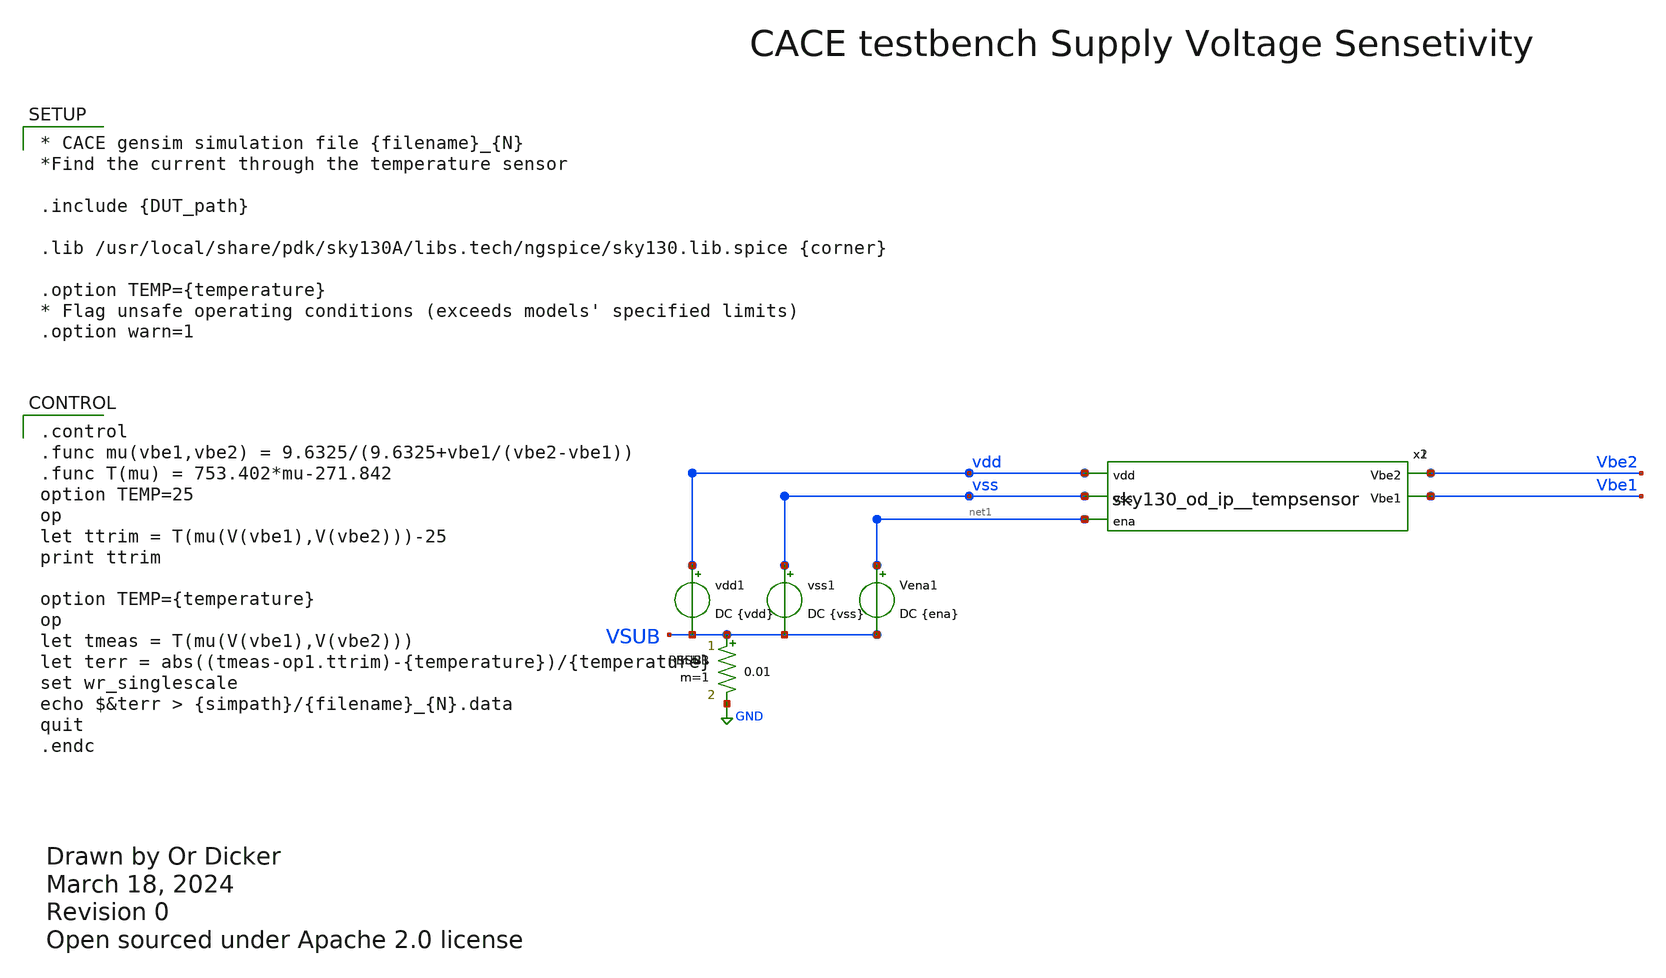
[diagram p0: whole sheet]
** sch_path: cace/supply_sens.sch
* Open sourced under Apache 2.0 license
**.subckt supply_sens
vss vss VSUB DC {vss}
vdd vdd VSUB DC {vdd}
RSUB VSUB GND 0.01 m=1
x1 vdd vss Vbe2 Vbe1 net1 sky130_od_ip__tempsensor
Vena net1 VSUB DC {ena}
vss1 vss VSUB DC {vss}
vdd1 vdd VSUB DC {vdd}
RSUB1 VSUB GND 0.01 m=1
x2 vdd vss Vbe2 Vbe1 net1 sky130_od_ip__tempsensor
Vena1 net1 VSUB DC {ena}
**** begin user architecture code

.control
.func mu(vbe1,vbe2) = 9.6325/(9.6325+vbe1/(vbe2-vbe1))
.func T(mu) = 753.402*mu-271.842
option TEMP=25
op
let ttrim = T(mu(V(vbe1),V(vbe2)))-25
print ttrim

option TEMP={temperature}
op
let tmeas = T(mu(V(vbe1),V(vbe2)))
let terr = abs((tmeas-op1.ttrim)-{temperature})/{temperature}
set wr_singlescale
echo $&terr > {simpath}/{filename}_{N}.data
quit
.endc



* CACE gensim simulation file {filename}_{N}
*Find the current through the temperature sensor

.include {DUT_path}

.lib /usr/local/share/pdk/sky130A/libs.tech/ngspice/sky130.lib.spice {corner}

.option TEMP={temperature}
* Flag unsafe operating conditions (exceeds models' specified limits)
.option warn=1


**** end user architecture code
**.ends

* expanding   symbol:  xschem/sky130_od_ip__tempsensor.sym # of pins=5
** sym_path: xschem/sky130_od_ip__tempsensor.sym
** sch_path: xschem/sky130_od_ip__tempsensor.sch
.subckt sky130_od_ip__tempsensor vdd vss Vbe2 Vbe1 ena
*.ipin vdd
*.ipin vss
*.opin Vbe2
*.opin Vbe1
*.ipin ena
XM12 net1 Vp vdd vdd sky130_fd_pr__pfet_01v8 L=1.2 W=1 nf=1 ad='int((nf+1)/2) * W/nf * 0.29' as='int((nf+2)/2)
+ * W/nf * 0.29' pd='2*int((nf+1)/2) * (W/nf + 0.29)' ps='2*int((nf+2)/2) * (W/nf + 0.29)' nrd='0.29 /
+ W' nrs='0.29 / W' sa=0 sb=0 sd=0 mult=5 m=5
XM13 net2 Vp vdd vdd sky130_fd_pr__pfet_01v8 L=1.2 W=1 nf=1 ad='int((nf+1)/2) * W/nf * 0.29' as='int((nf+2)/2)
+ * W/nf * 0.29' pd='2*int((nf+1)/2) * (W/nf + 0.29)' ps='2*int((nf+2)/2) * (W/nf + 0.29)' nrd='0.29 /
+ W' nrs='0.29 / W' sa=0 sb=0 sd=0 mult=1 m=1
XQ_BR vss net3 net1 sky130_fd_pr__pnp_05v5_W3p40L3p40 m=1
XQ_BL vss vss net4 sky130_fd_pr__pnp_05v5_W3p40L3p40 m=1
Rb net2 net4 5k m=1
Rb_5 net3 vss 1k m=1
XM11 net5 Vp vdd vdd sky130_fd_pr__pfet_01v8 L=1.2 W=1 nf=1 ad='int((nf+1)/2) * W/nf * 0.29' as='int((nf+2)/2)
+ * W/nf * 0.29' pd='2*int((nf+1)/2) * (W/nf + 0.29)' ps='2*int((nf+2)/2) * (W/nf + 0.29)' nrd='0.29 /
+ W' nrs='0.29 / W' sa=0 sb=0 sd=0 mult=2 m=2
XM6 net6 net2 net5 net5 sky130_fd_pr__pfet_01v8 L=1.2 W=10 nf=1 ad='int((nf+1)/2) * W/nf * 0.29' as='int((nf+2)/2)
+ * W/nf * 0.29' pd='2*int((nf+1)/2) * (W/nf + 0.29)' ps='2*int((nf+2)/2) * (W/nf + 0.29)' nrd='0.29 /
+ W' nrs='0.29 / W' sa=0 sb=0 sd=0 mult=1 m=1
XM5 net7 net1 net5 net5 sky130_fd_pr__pfet_01v8 L=1.2 W=10 nf=1 ad='int((nf+1)/2) * W/nf * 0.29' as='int((nf+2)/2)
+ * W/nf * 0.29' pd='2*int((nf+1)/2) * (W/nf + 0.29)' ps='2*int((nf+2)/2) * (W/nf + 0.29)' nrd='0.29 /
+ W' nrs='0.29 / W' sa=0 sb=0 sd=0 mult=1 m=1
XM2 net6 net7 vss vss sky130_fd_pr__nfet_01v8 L=1.2 W=10 nf=1 ad='int((nf+1)/2) * W/nf * 0.29' as='int((nf+2)/2)
+ * W/nf * 0.29' pd='2*int((nf+1)/2) * (W/nf + 0.29)' ps='2*int((nf+2)/2) * (W/nf + 0.29)' nrd='0.29 /
+ W' nrs='0.29 / W' sa=0 sb=0 sd=0 mult=1 m=1
XM1 net7 net7 vss vss sky130_fd_pr__nfet_01v8 L=1.2 W=10 nf=1 ad='int((nf+1)/2) * W/nf * 0.29' as='int((nf+2)/2)
+ * W/nf * 0.29' pd='2*int((nf+1)/2) * (W/nf + 0.29)' ps='2*int((nf+2)/2) * (W/nf + 0.29)' nrd='0.29 /
+ W' nrs='0.29 / W' sa=0 sb=0 sd=0 mult=1 m=1
XM9 net8 Vp vdd vdd sky130_fd_pr__pfet_01v8 L=1.2 W=1 nf=1 ad='int((nf+1)/2) * W/nf * 0.29' as='int((nf+2)/2)
+ * W/nf * 0.29' pd='2*int((nf+1)/2) * (W/nf + 0.29)' ps='2*int((nf+2)/2) * (W/nf + 0.29)' nrd='0.29 /
+ W' nrs='0.29 / W' sa=0 sb=0 sd=0 mult=1 m=1
XM10 Vp Vp vdd vdd sky130_fd_pr__pfet_01v8 L=1.2 W=1 nf=1 ad='int((nf+1)/2) * W/nf * 0.29' as='int((nf+2)/2)
+ * W/nf * 0.29' pd='2*int((nf+1)/2) * (W/nf + 0.29)' ps='2*int((nf+2)/2) * (W/nf + 0.29)' nrd='0.29 /
+ W' nrs='0.29 / W' sa=0 sb=0 sd=0 mult=4 m=4
XM7 Vp net8 net10 net10 sky130_fd_pr__nfet_01v8 L=1.2 W=10 nf=1 ad='int((nf+1)/2) * W/nf * 0.29' as='int((nf+2)/2)
+ * W/nf * 0.29' pd='2*int((nf+1)/2) * (W/nf + 0.29)' ps='2*int((nf+2)/2) * (W/nf + 0.29)' nrd='0.29 /
+ W' nrs='0.29 / W' sa=0 sb=0 sd=0 mult=1 m=1
XM8 net8 net8 net9 net9 sky130_fd_pr__nfet_01v8 L=1.2 W=10 nf=1 ad='int((nf+1)/2) * W/nf * 0.29' as='int((nf+2)/2)
+ * W/nf * 0.29' pd='2*int((nf+1)/2) * (W/nf + 0.29)' ps='2*int((nf+2)/2) * (W/nf + 0.29)' nrd='0.29 /
+ W' nrs='0.29 / W' sa=0 sb=0 sd=0 mult=1 m=1
XM3 net10 net6 vss vss sky130_fd_pr__nfet_01v8 L=1.2 W=10 nf=1 ad='int((nf+1)/2) * W/nf * 0.29' as='int((nf+2)/2)
+ * W/nf * 0.29' pd='2*int((nf+1)/2) * (W/nf + 0.29)' ps='2*int((nf+2)/2) * (W/nf + 0.29)' nrd='0.29 /
+ W' nrs='0.29 / W' sa=0 sb=0 sd=0 mult=4 m=4
XM4 net9 net9 vss vss sky130_fd_pr__nfet_01v8 L=1.2 W=1 nf=1 ad='int((nf+1)/2) * W/nf * 0.29' as='int((nf+2)/2)
+ * W/nf * 0.29' pd='2*int((nf+1)/2) * (W/nf + 0.29)' ps='2*int((nf+2)/2) * (W/nf + 0.29)' nrd='0.29 /
+ W' nrs='0.29 / W' sa=0 sb=0 sd=0 mult=20 m=20
XQ_BL1 vss vss Vbe1 sky130_fd_pr__pnp_05v5_W3p40L3p40 m=1
XQ_BR1 vss vss Vbe2 sky130_fd_pr__pnp_05v5_W3p40L3p40 m=1
XM14 Vbe1 Vp vdd vdd sky130_fd_pr__pfet_01v8 L=1.2 W=1 nf=1 ad='int((nf+1)/2) * W/nf * 0.29' as='int((nf+2)/2)
+ * W/nf * 0.29' pd='2*int((nf+1)/2) * (W/nf + 0.29)' ps='2*int((nf+2)/2) * (W/nf + 0.29)' nrd='0.29 /
+ W' nrs='0.29 / W' sa=0 sb=0 sd=0 mult=1 m=1
XM15 Vbe2 Vp vdd vdd sky130_fd_pr__pfet_01v8 L=1.2 W=1 nf=1 ad='int((nf+1)/2) * W/nf * 0.29' as='int((nf+2)/2)
+ * W/nf * 0.29' pd='2*int((nf+1)/2) * (W/nf + 0.29)' ps='2*int((nf+2)/2) * (W/nf + 0.29)' nrd='0.29 /
+ W' nrs='0.29 / W' sa=0 sb=0 sd=0 mult=5 m=5
XM16 Vp ena vdd vdd sky130_fd_pr__pfet_01v8 L=1.2 W=10 nf=1 ad='int((nf+1)/2) * W/nf * 0.29' as='int((nf+2)/2)
+ * W/nf * 0.29' pd='2*int((nf+1)/2) * (W/nf + 0.29)' ps='2*int((nf+2)/2) * (W/nf + 0.29)' nrd='0.29 /
+ W' nrs='0.29 / W' sa=0 sb=0 sd=0 mult=1 m=1
.ends

.GLOBAL GND
.end
